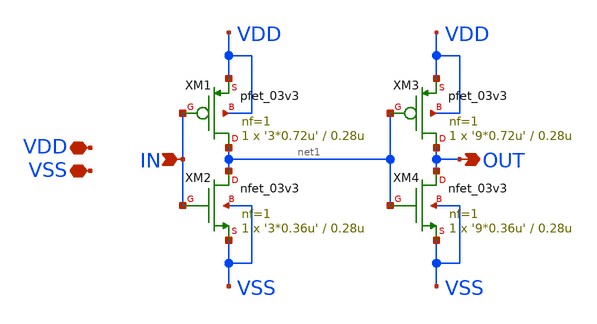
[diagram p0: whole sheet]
** sch_path: CAD6/sign_extend.sch
**.subckt sign_extend VDD VSS IN OUT
*.iopin VDD
*.iopin VSS
*.ipin IN
*.opin OUT
XM1 net1 IN VDD VDD pfet_03v3 L=0.28u W='3*0.72u' nf=1 ad='int((nf+1)/2) * W/nf * 0.18u' as='int((nf+2)/2) * W/nf * 0.18u'
+ pd='2*int((nf+1)/2) * (W/nf + 0.18u)' ps='2*int((nf+2)/2) * (W/nf + 0.18u)' nrd='0.18u / W' nrs='0.18u / W'
+ sa=0 sb=0 sd=0 m=1
XM2 net1 IN VSS VSS nfet_03v3 L=0.28u W='3*0.36u' nf=1 ad='int((nf+1)/2) * W/nf * 0.18u' as='int((nf+2)/2) * W/nf * 0.18u'
+ pd='2*int((nf+1)/2) * (W/nf + 0.18u)' ps='2*int((nf+2)/2) * (W/nf + 0.18u)' nrd='0.18u / W' nrs='0.18u / W'
+ sa=0 sb=0 sd=0 m=1
XM3 OUT net1 VDD VDD pfet_03v3 L=0.28u W='9*0.72u' nf=1 ad='int((nf+1)/2) * W/nf * 0.18u' as='int((nf+2)/2) * W/nf * 0.18u'
+ pd='2*int((nf+1)/2) * (W/nf + 0.18u)' ps='2*int((nf+2)/2) * (W/nf + 0.18u)' nrd='0.18u / W' nrs='0.18u / W'
+ sa=0 sb=0 sd=0 m=1
XM4 OUT net1 VSS VSS nfet_03v3 L=0.28u W='9*0.36u' nf=1 ad='int((nf+1)/2) * W/nf * 0.18u' as='int((nf+2)/2) * W/nf * 0.18u'
+ pd='2*int((nf+1)/2) * (W/nf + 0.18u)' ps='2*int((nf+2)/2) * (W/nf + 0.18u)' nrd='0.18u / W' nrs='0.18u / W'
+ sa=0 sb=0 sd=0 m=1
**.ends
.end
